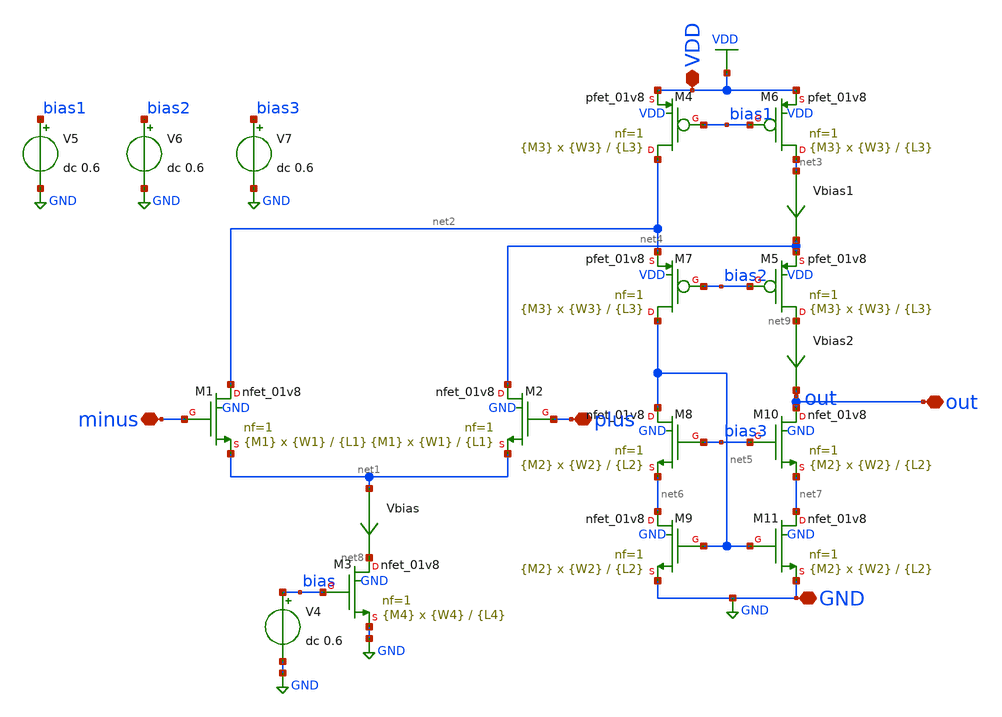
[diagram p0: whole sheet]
** sch_path: xschem/op3.sch
**.subckt op3 VDD GND minus plus out
*.iopin VDD
*.iopin GND
*.iopin minus
*.iopin plus
*.iopin out
V4 bias GND dc 0.6
XM1 net2 minus net1 GND sky130_fd_pr__nfet_01v8 L={L1} W={W1} nf=1 ad='int((nf+1)/2) * W/nf * 0.29' as='int((nf+2)/2) * W/nf * 0.29'
+ pd='2*int((nf+1)/2) * (W/nf + 0.29)' ps='2*int((nf+2)/2) * (W/nf + 0.29)' nrd='0.29 / W' nrs='0.29 / W'
+ sa=0 sb=0 sd=0 mult={M1} m={M1}
XM3 net8 bias GND GND sky130_fd_pr__nfet_01v8 L={L4} W={W4} nf=1 ad='int((nf+1)/2) * W/nf * 0.29' as='int((nf+2)/2) * W/nf * 0.29'
+ pd='2*int((nf+1)/2) * (W/nf + 0.29)' ps='2*int((nf+2)/2) * (W/nf + 0.29)' nrd='0.29 / W' nrs='0.29 / W'
+ sa=0 sb=0 sd=0 mult={M4} m={M4}
Vbias net1 net8 0
.save i(vbias)
XM2 net4 plus net1 GND sky130_fd_pr__nfet_01v8 L={L1} W={W1} nf=1 ad='int((nf+1)/2) * W/nf * 0.29' as='int((nf+2)/2) * W/nf * 0.29'
+ pd='2*int((nf+1)/2) * (W/nf + 0.29)' ps='2*int((nf+2)/2) * (W/nf + 0.29)' nrd='0.29 / W' nrs='0.29 / W'
+ sa=0 sb=0 sd=0 mult={M1} m={M1}
XM7 net5 bias2 net2 VDD sky130_fd_pr__pfet_01v8 L={L3} W={W3} nf=1 ad='int((nf+1)/2) * W/nf * 0.29' as='int((nf+2)/2) * W/nf * 0.29'
+ pd='2*int((nf+1)/2) * (W/nf + 0.29)' ps='2*int((nf+2)/2) * (W/nf + 0.29)' nrd='0.29 / W' nrs='0.29 / W'
+ sa=0 sb=0 sd=0 mult={M3} m={M3}
XM8 net5 bias3 net6 GND sky130_fd_pr__nfet_01v8 L={L2} W={W2} nf=1 ad='int((nf+1)/2) * W/nf * 0.29' as='int((nf+2)/2) * W/nf * 0.29'
+ pd='2*int((nf+1)/2) * (W/nf + 0.29)' ps='2*int((nf+2)/2) * (W/nf + 0.29)' nrd='0.29 / W' nrs='0.29 / W'
+ sa=0 sb=0 sd=0 mult={M2} m={M2}
XM9 net6 net5 GND GND sky130_fd_pr__nfet_01v8 L={L2} W={W2} nf=1 ad='int((nf+1)/2) * W/nf * 0.29' as='int((nf+2)/2) * W/nf * 0.29'
+ pd='2*int((nf+1)/2) * (W/nf + 0.29)' ps='2*int((nf+2)/2) * (W/nf + 0.29)' nrd='0.29 / W' nrs='0.29 / W'
+ sa=0 sb=0 sd=0 mult={M2} m={M2}
XM10 out bias3 net7 GND sky130_fd_pr__nfet_01v8 L={L2} W={W2} nf=1 ad='int((nf+1)/2) * W/nf * 0.29' as='int((nf+2)/2) * W/nf * 0.29'
+ pd='2*int((nf+1)/2) * (W/nf + 0.29)' ps='2*int((nf+2)/2) * (W/nf + 0.29)' nrd='0.29 / W' nrs='0.29 / W'
+ sa=0 sb=0 sd=0 mult={M2} m={M2}
XM11 net7 net5 GND GND sky130_fd_pr__nfet_01v8 L={L2} W={W2} nf=1 ad='int((nf+1)/2) * W/nf * 0.29' as='int((nf+2)/2) * W/nf * 0.29'
+ pd='2*int((nf+1)/2) * (W/nf + 0.29)' ps='2*int((nf+2)/2) * (W/nf + 0.29)' nrd='0.29 / W' nrs='0.29 / W'
+ sa=0 sb=0 sd=0 mult={M2} m={M2}
V5 bias1 GND dc 0.6
V6 bias2 GND dc 0.6
V7 bias3 GND dc 0.6
Vbias1 net3 net4 0
.save i(vbias1)
Vbias2 net9 out 0
.save i(vbias2)
XM4 net2 bias1 VDD VDD sky130_fd_pr__pfet_01v8 L={L3} W={W3} nf=1 ad='int((nf+1)/2) * W/nf * 0.29' as='int((nf+2)/2) * W/nf * 0.29'
+ pd='2*int((nf+1)/2) * (W/nf + 0.29)' ps='2*int((nf+2)/2) * (W/nf + 0.29)' nrd='0.29 / W' nrs='0.29 / W'
+ sa=0 sb=0 sd=0 mult={M3} m={M3}
XM5 net9 bias2 net4 VDD sky130_fd_pr__pfet_01v8 L={L3} W={W3} nf=1 ad='int((nf+1)/2) * W/nf * 0.29' as='int((nf+2)/2) * W/nf * 0.29'
+ pd='2*int((nf+1)/2) * (W/nf + 0.29)' ps='2*int((nf+2)/2) * (W/nf + 0.29)' nrd='0.29 / W' nrs='0.29 / W'
+ sa=0 sb=0 sd=0 mult={M3} m={M3}
XM6 net3 bias1 VDD VDD sky130_fd_pr__pfet_01v8 L={L3} W={W3} nf=1 ad='int((nf+1)/2) * W/nf * 0.29' as='int((nf+2)/2) * W/nf * 0.29'
+ pd='2*int((nf+1)/2) * (W/nf + 0.29)' ps='2*int((nf+2)/2) * (W/nf + 0.29)' nrd='0.29 / W' nrs='0.29 / W'
+ sa=0 sb=0 sd=0 mult={M3} m={M3}
**** begin user architecture code


**diffpair**
.param L1=1
.param W1=5
.param M1=1

**PMOS**
.param L2=1
.param W2=2
.param M2=1

**NMOS**
.param L3=10
.param W3=1
.param M3=1

**Current control**
.param L4=5
.param W4=2.5
.param M4=1


**** end user architecture code
**.ends
.GLOBAL GND
.GLOBAL VDD
.end
